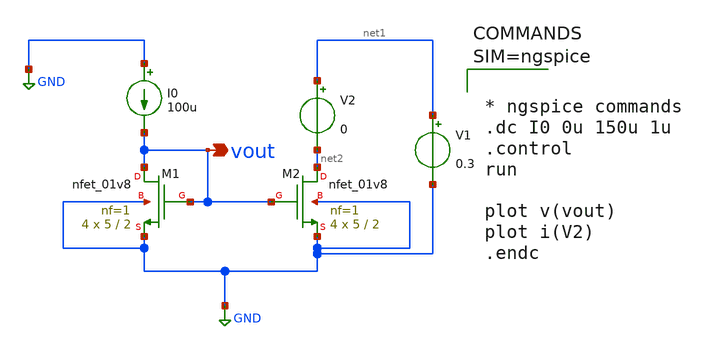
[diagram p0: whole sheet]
** sch_path: xschem/current_mirror_in_impe.sch
**.subckt current_mirror_in_impe vout
*.opin vout
XM2 net2 vout GND GND sky130_fd_pr__nfet_01v8 L=2 W=5 nf=1 ad='int((1 + 1)/2) * 5 / 1 * 0.29' as='int((1 + 2)/2) * 5 / 1 * 0.29'
+ pd='2*int((1 + 1)/2) * (5 / 1 + 0.29)' ps='2*int((1 + 2)/2) * (5 / 1 + 0.29)' nrd='0.29 / 5 ' nrs='0.29 / 5 '
+ sa=0 sb=0 sd=0 mult=4 m=4
XM1 vout vout GND GND sky130_fd_pr__nfet_01v8 L=2 W=5 nf=1 ad='int((1 + 1)/2) * 5 / 1 * 0.29' as='int((1 + 2)/2) * 5 / 1 * 0.29'
+ pd='2*int((1 + 1)/2) * (5 / 1 + 0.29)' ps='2*int((1 + 2)/2) * (5 / 1 + 0.29)' nrd='0.29 / 5 ' nrs='0.29 / 5 '
+ sa=0 sb=0 sd=0 mult=4 m=4
I0 GND vout 100u
V1 net1 GND 0.3
V2 net1 net2 0
**** begin user architecture code

** opencircuitdesign pdks install
.lib $::SKYWATER_MODELS/sky130.lib.spice tt




* ngspice commands
.dc I0 0u 150u 1u
.control
run

plot v(vout)
plot i(V2)
.endc



**** end user architecture code
**.ends
.GLOBAL GND
.end
